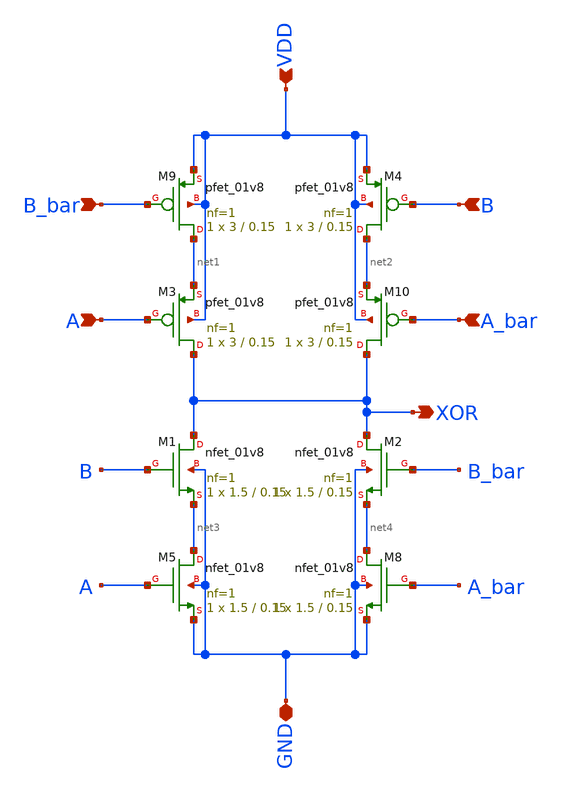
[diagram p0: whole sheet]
** sch_path: skywater_stuff/CMOS_XOR.sch
**.subckt CMOS_XOR A A_bar B B_bar XOR GND VDD
*.ipin A
*.ipin A_bar
*.ipin B
*.ipin B_bar
*.opin XOR
*.iopin GND
*.ipin VDD
XM8 net4 A_bar GND GND sky130_fd_pr__nfet_01v8 L=0.15 W=1.5 nf=1 ad='int((nf+1)/2) * W/nf * 0.29' as='int((nf+2)/2) * W/nf * 0.29'
+ pd='2*int((nf+1)/2) * (W/nf + 0.29)' ps='2*int((nf+2)/2) * (W/nf + 0.29)' nrd='0.29 / W' nrs='0.29 / W'
+ sa=0 sb=0 sd=0 mult=1 m=1
XM1 XOR B net3 GND sky130_fd_pr__nfet_01v8 L=0.15 W=1.5 nf=1 ad='int((nf+1)/2) * W/nf * 0.29' as='int((nf+2)/2) * W/nf * 0.29'
+ pd='2*int((nf+1)/2) * (W/nf + 0.29)' ps='2*int((nf+2)/2) * (W/nf + 0.29)' nrd='0.29 / W' nrs='0.29 / W'
+ sa=0 sb=0 sd=0 mult=1 m=1
XM3 XOR A net1 VDD sky130_fd_pr__pfet_01v8 L=0.15 W=3 nf=1 ad='int((nf+1)/2) * W/nf * 0.29' as='int((nf+2)/2) * W/nf * 0.29'
+ pd='2*int((nf+1)/2) * (W/nf + 0.29)' ps='2*int((nf+2)/2) * (W/nf + 0.29)' nrd='0.29 / W' nrs='0.29 / W'
+ sa=0 sb=0 sd=0 mult=1 m=1
XM4 net2 B VDD VDD sky130_fd_pr__pfet_01v8 L=0.15 W=3 nf=1 ad='int((nf+1)/2) * W/nf * 0.29' as='int((nf+2)/2) * W/nf * 0.29'
+ pd='2*int((nf+1)/2) * (W/nf + 0.29)' ps='2*int((nf+2)/2) * (W/nf + 0.29)' nrd='0.29 / W' nrs='0.29 / W'
+ sa=0 sb=0 sd=0 mult=1 m=1
XM9 net1 B_bar VDD VDD sky130_fd_pr__pfet_01v8 L=0.15 W=3 nf=1 ad='int((nf+1)/2) * W/nf * 0.29' as='int((nf+2)/2) * W/nf * 0.29'
+ pd='2*int((nf+1)/2) * (W/nf + 0.29)' ps='2*int((nf+2)/2) * (W/nf + 0.29)' nrd='0.29 / W' nrs='0.29 / W'
+ sa=0 sb=0 sd=0 mult=1 m=1
XM2 XOR B_bar net4 GND sky130_fd_pr__nfet_01v8 L=0.15 W=1.5 nf=1 ad='int((nf+1)/2) * W/nf * 0.29' as='int((nf+2)/2) * W/nf * 0.29'
+ pd='2*int((nf+1)/2) * (W/nf + 0.29)' ps='2*int((nf+2)/2) * (W/nf + 0.29)' nrd='0.29 / W' nrs='0.29 / W'
+ sa=0 sb=0 sd=0 mult=1 m=1
XM5 net3 A GND GND sky130_fd_pr__nfet_01v8 L=0.15 W=1.5 nf=1 ad='int((nf+1)/2) * W/nf * 0.29' as='int((nf+2)/2) * W/nf * 0.29'
+ pd='2*int((nf+1)/2) * (W/nf + 0.29)' ps='2*int((nf+2)/2) * (W/nf + 0.29)' nrd='0.29 / W' nrs='0.29 / W'
+ sa=0 sb=0 sd=0 mult=1 m=1
XM10 XOR A_bar net2 VDD sky130_fd_pr__pfet_01v8 L=0.15 W=3 nf=1 ad='int((nf+1)/2) * W/nf * 0.29' as='int((nf+2)/2) * W/nf * 0.29'
+ pd='2*int((nf+1)/2) * (W/nf + 0.29)' ps='2*int((nf+2)/2) * (W/nf + 0.29)' nrd='0.29 / W' nrs='0.29 / W'
+ sa=0 sb=0 sd=0 mult=1 m=1
**.ends
.end
